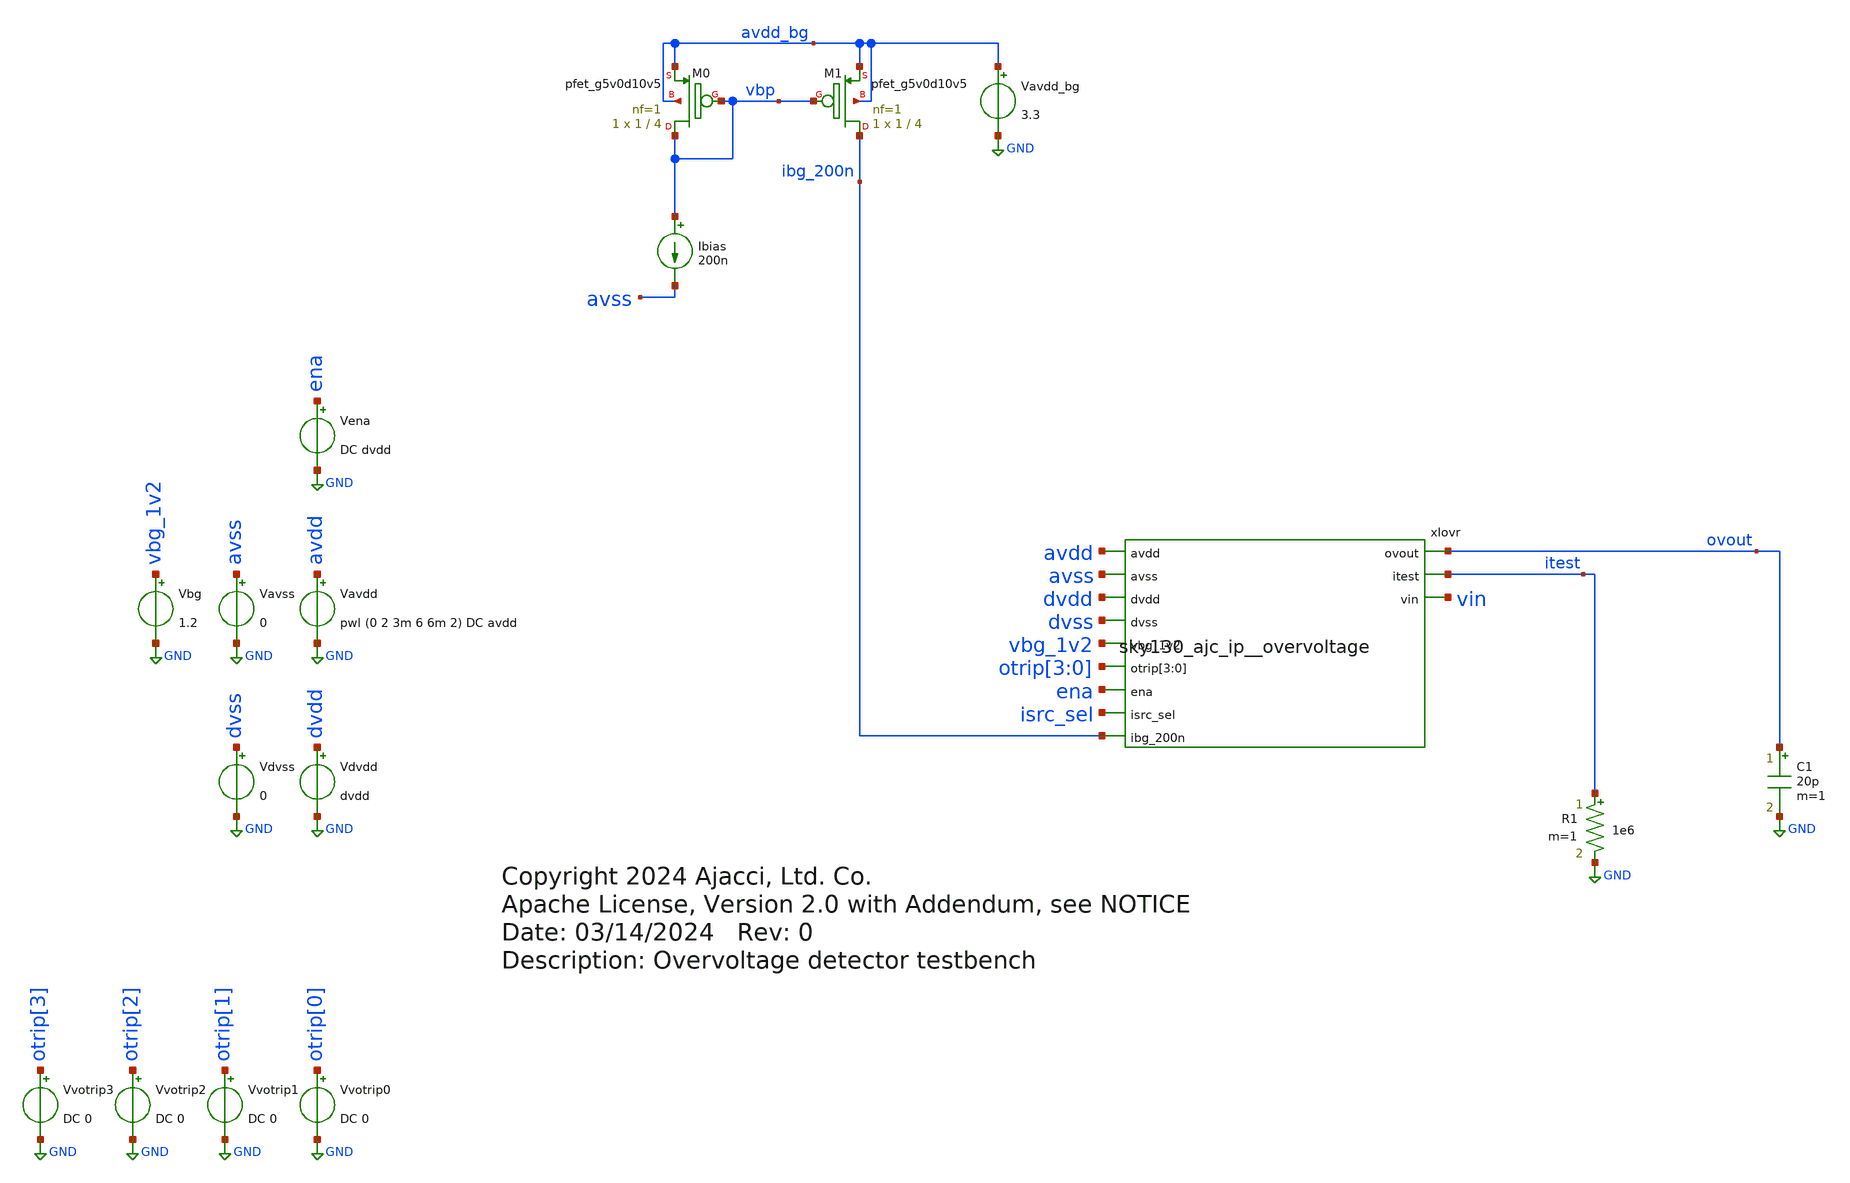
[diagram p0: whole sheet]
** sch_path: xschem/sky130_ajc_ip__overvoltage_tb.sch
* Copyright 2024 Ajacci, Ltd. Co.
* Apache License, Version 2.0 with Addendum, see NOTICE
**.subckt sky130_ajc_ip__overvoltage_tb
Vavss avss GND 0
Vena ena GND DC dvdd
Vavdd avdd GND pwl (0 2 3m 6 6m 2) DC avdd
.save i(vavdd)
Vbg vbg_1v2 GND 1.2
Ibias vbp avss 200n
XM1 ibg_200n vbp avdd_bg avdd_bg sky130_fd_pr__pfet_g5v0d10v5 L=4 W=1 nf=1 ad='int((nf+1)/2) * W/nf * 0.29'
+ as='int((nf+2)/2) * W/nf * 0.29' pd='2*int((nf+1)/2) * (W/nf + 0.29)' ps='2*int((nf+2)/2) * (W/nf + 0.29)'
+ nrd='0.29 / W' nrs='0.29 / W' sa=0 sb=0 sd=0 mult=1 m=1
XM0 vbp vbp avdd_bg avdd_bg sky130_fd_pr__pfet_g5v0d10v5 L=4 W=1 nf=1 ad='int((nf+1)/2) * W/nf * 0.29'
+ as='int((nf+2)/2) * W/nf * 0.29' pd='2*int((nf+1)/2) * (W/nf + 0.29)' ps='2*int((nf+2)/2) * (W/nf + 0.29)'
+ nrd='0.29 / W' nrs='0.29 / W' sa=0 sb=0 sd=0 mult=1 m=1
Vdvss dvss GND 0
Vdvdd dvdd GND dvdd
.save i(vdvdd)
R1 itest GND 1e6 m=1
C1 ovout GND 20p m=1
xIovr avdd avss dvdd dvss vbg_1v2 ovout itest otrip[3] otrip[2] otrip[1] otrip[0] vin ena isrc_sel
+ ibg_200n sky130_ajc_ip__overvoltage
Vvotrip0 otrip[0] GND DC 0
Vvotrip1 otrip[1] GND DC 0
Vvotrip2 otrip[2] GND DC 0
Vvotrip3 otrip[3] GND DC 0
Vavdd_bg avdd_bg GND 3.3
.save i(vavdd_bg)
**** begin user architecture code


.param avdd=3.3
.param dvdd=1.8
.csparam dvdd2=dvdd/2

.lib libs.tech/ngspice/sky130.lib.spice tt
.include libs.ref/sky130_fd_sc_hvl/spice/sky130_fd_sc_hvl.spice
.include libs.ref/sky130_fd_sc_hd/spice/sky130_fd_sc_hd.spice

*dig pull up/down to set test bits
R000 ena dvdd 1e9
R001 isrc_sel dvss 1e9

.option reltol 5e-5

.temp 27
.save all

.control
*op
*print ovout vin
tran 2u 6m
*plot ovout itest avdd ena vbg_1v2 vin xiovr.xiana.dcomp xiovr.xiana.dcomp_filt
*plot i(Vavdd) i(Vdvdd)
plot ovout avdd ena*0.5

meas tran vtrip_r find v(avdd) when v(ovout)=$&dvdd2 td=300u rise=1
meas tran vtrip_f find v(avdd) when v(ovout)=$&dvdd2 td=3m fall=1
let accu = ($&vtrip_r + $&vtrip_f)/2
let hyst = $&vtrip_r - $&vtrip_f
print $&accu
print $&hyst
.endc


**** end user architecture code
**.ends
.GLOBAL GND
.end
